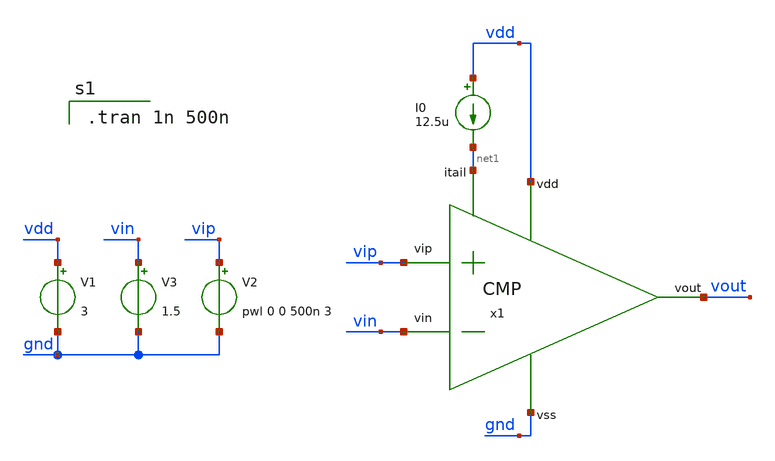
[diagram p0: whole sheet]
** sch_path: design/JNW_AVV_SKY130A/TB_CMP.sch
**.subckt TB_CMP
I0 vdd net1 12.5u
V1 vdd gnd 3
V2 vip gnd pwl 0 0 500n 3
V3 vin gnd 1.5
x1 vdd net1 vout vin vip gnd CMP
**** begin user architecture code

.tran 1n 500n

**** end user architecture code
**.ends
.end
